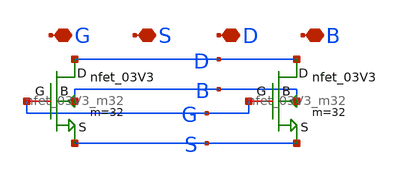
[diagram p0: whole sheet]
** sch_path: DAC_PAKISTAN_01/Pakistan1_Xschem/nfet_03V3_m64.sch
**.subckt nfet_03V3_m64 G S D B
*.iopin G
*.iopin S
*.iopin D
*.iopin B
x1 S D B G nfet_03V3_m32
x2 S D B G nfet_03V3_m32
**.ends
.end
